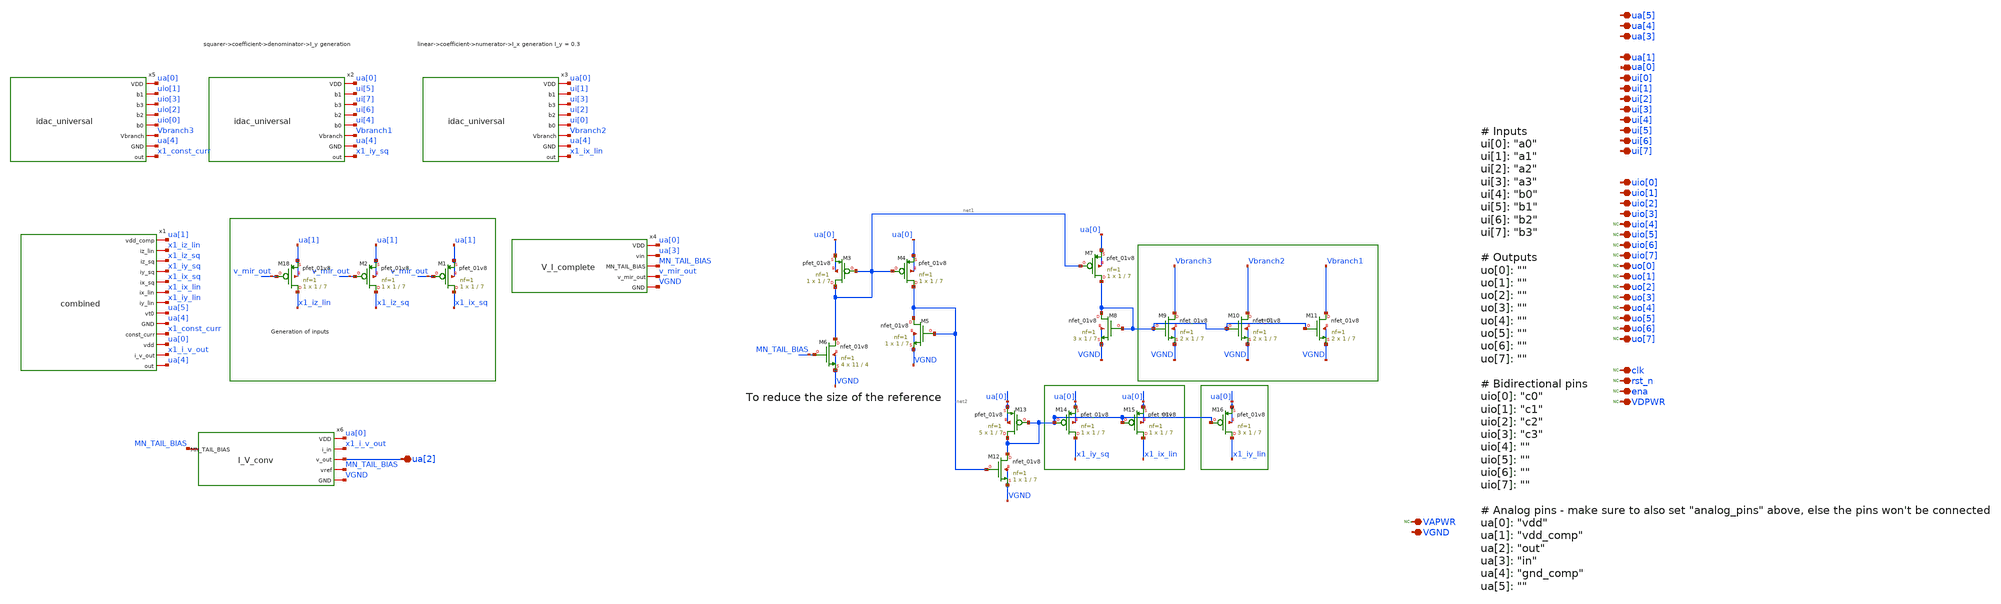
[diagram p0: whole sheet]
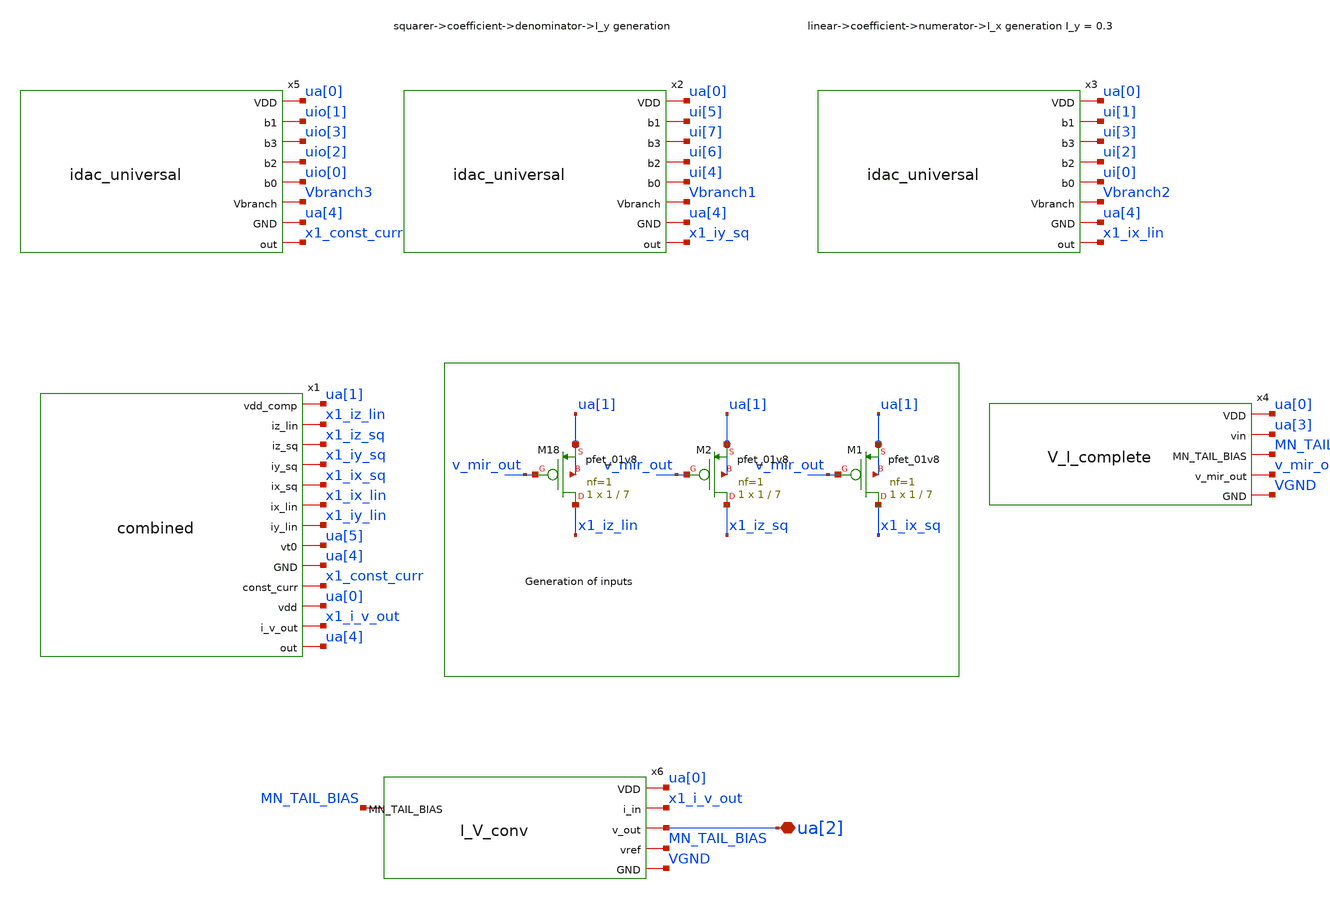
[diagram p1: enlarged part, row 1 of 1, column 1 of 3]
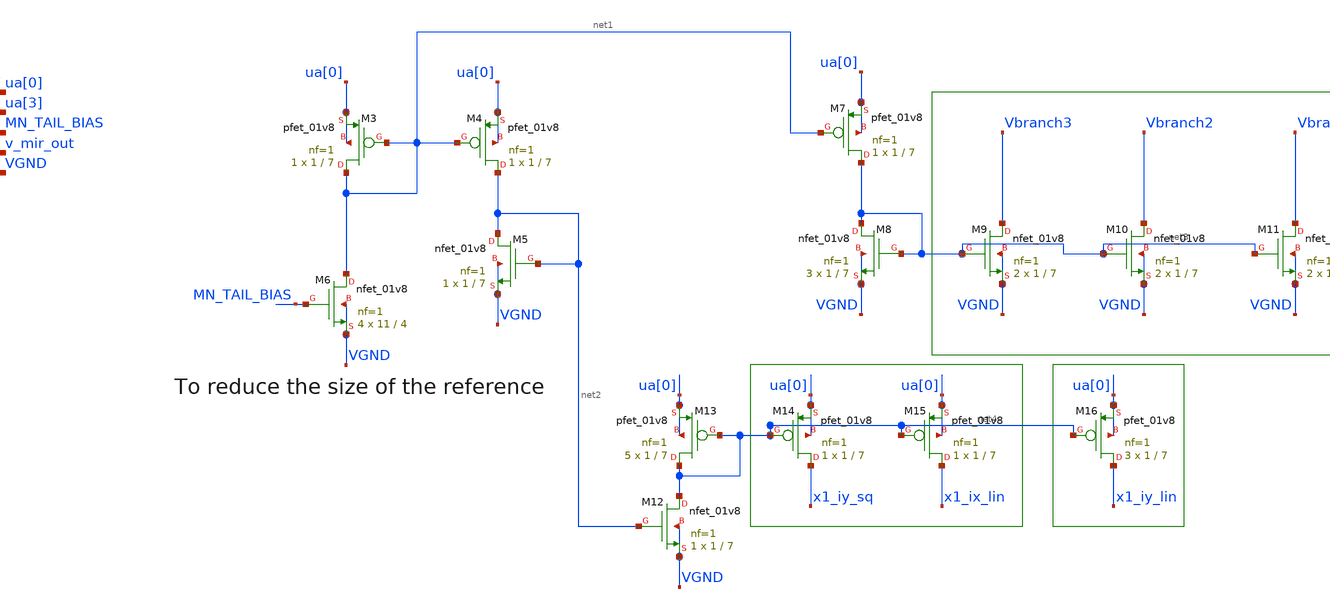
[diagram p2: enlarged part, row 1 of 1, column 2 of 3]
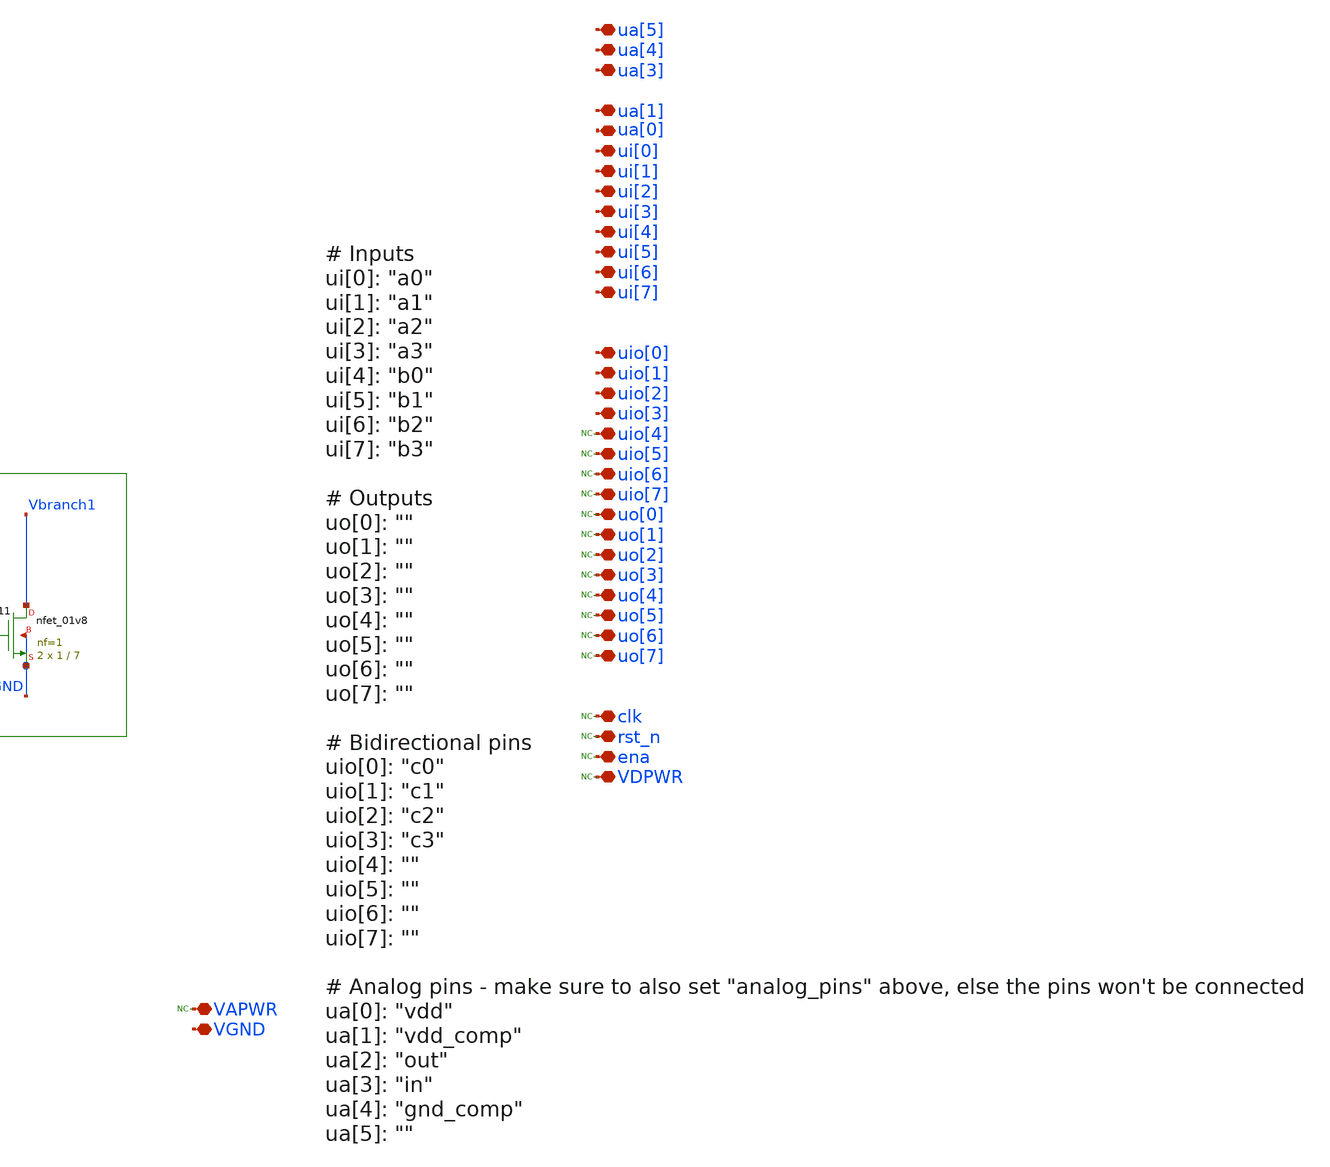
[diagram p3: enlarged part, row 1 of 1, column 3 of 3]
** sch_path: xschem/top/tt_um_psquared_analog_compute.sch
**.subckt tt_um_psquared_analog_compute ui[4] ui[5] ui[6] ui[7] uio[0] uio[1] uio[2] uio[3] uio[4]
*+ uio[5] uio[6] uio[7] uo[0] uo[1] uo[2] uo[3] uo[4] uo[5] uo[6] uo[7] clk rst_n ena ua[4] ua[5] ui[0] ui[3]
*+ ui[1] ui[2] VDPWR ua[3] ua[1] ua[0] VAPWR VGND ua[2]
*.iopin ui[4]
*.iopin ui[5]
*.iopin ui[6]
*.iopin ui[7]
*.iopin uio[0]
*.iopin uio[1]
*.iopin uio[2]
*.iopin uio[3]
*.iopin uio[4]
*.iopin uio[5]
*.iopin uio[6]
*.iopin uio[7]
*.iopin uo[0]
*.iopin uo[1]
*.iopin uo[2]
*.iopin uo[3]
*.iopin uo[4]
*.iopin uo[5]
*.iopin uo[6]
*.iopin uo[7]
*.iopin clk
*.iopin rst_n
*.iopin ena
*.iopin ua[4]
*.iopin ua[5]
*.iopin ui[0]
*.iopin ui[3]
*.iopin ui[1]
*.iopin ui[2]
*.iopin VDPWR
*.iopin ua[3]
*.iopin ua[1]
*.iopin ua[0]
*.iopin VAPWR
*.iopin VGND
*.iopin ua[2]
* noconn uio[4]
* noconn uio[5]
* noconn uio[6]
* noconn uio[7]
* noconn uo[0]
* noconn uo[1]
* noconn uo[2]
* noconn uo[3]
* noconn uo[4]
* noconn uo[5]
* noconn uo[6]
* noconn uo[7]
* noconn clk
* noconn rst_n
* noconn ena
* noconn VDPWR
x5 ua[0] uio[1] uio[3] uio[2] uio[0] Vbranch3 ua[4] x1_const_curr idac_universal
x2 ua[0] ui[5] ui[7] ui[6] ui[4] Vbranch1 ua[4] x1_iy_sq idac_universal
x3 ua[0] ui[1] ui[3] ui[2] ui[0] Vbranch2 ua[4] x1_ix_lin idac_universal
x1 ua[1] x1_iz_lin x1_iz_sq x1_iy_sq x1_ix_sq x1_ix_lin x1_iy_lin ua[5] ua[4] x1_const_curr ua[0]
+ x1_i_v_out ua[4] combined
x6 ua[0] x1_i_v_out ua[2] MN_TAIL_BIAS VGND MN_TAIL_BIAS I_V_conv
x4 ua[0] ua[3] MN_TAIL_BIAS v_mir_out VGND V_I_complete
XM6 net1 MN_TAIL_BIAS VGND VGND sky130_fd_pr__nfet_01v8 L=4 W=11 nf=1 ad='int((1 + 1)/2) * 11 / 1 * 0.29'
+ as='int((1 + 2)/2) * 11 / 1 * 0.29' pd='2*int((1 + 1)/2) * (11 / 1 + 0.29)' ps='2*int((1 + 2)/2) * (11 / 1 + 0.29)'
+ nrd='0.29 / 11 ' nrs='0.29 / 11 ' sa=0 sb=0 sd=0 mult=4 m=4
XM5 net2 net2 VGND VGND sky130_fd_pr__nfet_01v8 L=7 W=1 nf=1 ad='int((1 + 1)/2) * 1 / 1 * 0.29' as='int((1 + 2)/2) * 1 / 1 * 0.29'
+ pd='2*int((1 + 1)/2) * (1 / 1 + 0.29)' ps='2*int((1 + 2)/2) * (1 / 1 + 0.29)' nrd='0.29 / 1 ' nrs='0.29 / 1 '
+ sa=0 sb=0 sd=0 mult=1 m=1
XM12 net4 net2 VGND VGND sky130_fd_pr__nfet_01v8 L=7 W=1 nf=1 ad='int((1 + 1)/2) * 1 / 1 * 0.29' as='int((1 + 2)/2) * 1 / 1 * 0.29'
+ pd='2*int((1 + 1)/2) * (1 / 1 + 0.29)' ps='2*int((1 + 2)/2) * (1 / 1 + 0.29)' nrd='0.29 / 1 ' nrs='0.29 / 1 '
+ sa=0 sb=0 sd=0 mult=1 m=1
XM8 net3 net3 VGND VGND sky130_fd_pr__nfet_01v8 L=7 W=1 nf=1 ad='int((1 + 1)/2) * 1 / 1 * 0.29' as='int((1 + 2)/2) * 1 / 1 * 0.29'
+ pd='2*int((1 + 1)/2) * (1 / 1 + 0.29)' ps='2*int((1 + 2)/2) * (1 / 1 + 0.29)' nrd='0.29 / 1 ' nrs='0.29 / 1 '
+ sa=0 sb=0 sd=0 mult=3 m=3
XM9 Vbranch3 net3 VGND VGND sky130_fd_pr__nfet_01v8 L=7 W=1 nf=1 ad='int((1 + 1)/2) * 1 / 1 * 0.29' as='int((1 + 2)/2) * 1 / 1 * 0.29'
+ pd='2*int((1 + 1)/2) * (1 / 1 + 0.29)' ps='2*int((1 + 2)/2) * (1 / 1 + 0.29)' nrd='0.29 / 1 ' nrs='0.29 / 1 '
+ sa=0 sb=0 sd=0 mult=2 m=2
XM11 Vbranch1 net3 VGND VGND sky130_fd_pr__nfet_01v8 L=7 W=1 nf=1 ad='int((1 + 1)/2) * 1 / 1 * 0.29'
+ as='int((1 + 2)/2) * 1 / 1 * 0.29' pd='2*int((1 + 1)/2) * (1 / 1 + 0.29)' ps='2*int((1 + 2)/2) * (1 / 1 + 0.29)'
+ nrd='0.29 / 1 ' nrs='0.29 / 1 ' sa=0 sb=0 sd=0 mult=2 m=2
XM10 Vbranch2 net3 VGND VGND sky130_fd_pr__nfet_01v8 L=7 W=1 nf=1 ad='int((1 + 1)/2) * 1 / 1 * 0.29'
+ as='int((1 + 2)/2) * 1 / 1 * 0.29' pd='2*int((1 + 1)/2) * (1 / 1 + 0.29)' ps='2*int((1 + 2)/2) * (1 / 1 + 0.29)'
+ nrd='0.29 / 1 ' nrs='0.29 / 1 ' sa=0 sb=0 sd=0 mult=2 m=2
XM3 net1 net1 ua[0] ua[0] sky130_fd_pr__pfet_01v8 L=7 W=1 nf=1 ad='int((nf+1)/2) * W/nf * 0.29' as='int((nf+2)/2) * W/nf * 0.29'
+ pd='2*int((nf+1)/2) * (W/nf + 0.29)' ps='2*int((nf+2)/2) * (W/nf + 0.29)' nrd='0.29 / W' nrs='0.29 / W'
+ sa=0 sb=0 sd=0 mult=1 m=1
XM4 net2 net1 ua[0] ua[0] sky130_fd_pr__pfet_01v8 L=7 W=1 nf=1 ad='int((nf+1)/2) * W/nf * 0.29' as='int((nf+2)/2) * W/nf * 0.29'
+ pd='2*int((nf+1)/2) * (W/nf + 0.29)' ps='2*int((nf+2)/2) * (W/nf + 0.29)' nrd='0.29 / W' nrs='0.29 / W'
+ sa=0 sb=0 sd=0 mult=1 m=1
XM7 net3 net1 ua[0] ua[0] sky130_fd_pr__pfet_01v8 L=7 W=1 nf=1 ad='int((nf+1)/2) * W/nf * 0.29' as='int((nf+2)/2) * W/nf * 0.29'
+ pd='2*int((nf+1)/2) * (W/nf + 0.29)' ps='2*int((nf+2)/2) * (W/nf + 0.29)' nrd='0.29 / W' nrs='0.29 / W'
+ sa=0 sb=0 sd=0 mult=1 m=1
XM16 x1_iy_lin net4 ua[0] ua[0] sky130_fd_pr__pfet_01v8 L=7 W=1 nf=1 ad='int((nf+1)/2) * W/nf * 0.29'
+ as='int((nf+2)/2) * W/nf * 0.29' pd='2*int((nf+1)/2) * (W/nf + 0.29)' ps='2*int((nf+2)/2) * (W/nf + 0.29)'
+ nrd='0.29 / W' nrs='0.29 / W' sa=0 sb=0 sd=0 mult=3 m=3
XM15 x1_ix_lin net4 ua[0] ua[0] sky130_fd_pr__pfet_01v8 L=7 W=1 nf=1 ad='int((nf+1)/2) * W/nf * 0.29'
+ as='int((nf+2)/2) * W/nf * 0.29' pd='2*int((nf+1)/2) * (W/nf + 0.29)' ps='2*int((nf+2)/2) * (W/nf + 0.29)'
+ nrd='0.29 / W' nrs='0.29 / W' sa=0 sb=0 sd=0 mult=1 m=1
XM14 x1_iy_sq net4 ua[0] ua[0] sky130_fd_pr__pfet_01v8 L=7 W=1 nf=1 ad='int((nf+1)/2) * W/nf * 0.29'
+ as='int((nf+2)/2) * W/nf * 0.29' pd='2*int((nf+1)/2) * (W/nf + 0.29)' ps='2*int((nf+2)/2) * (W/nf + 0.29)'
+ nrd='0.29 / W' nrs='0.29 / W' sa=0 sb=0 sd=0 mult=1 m=1
XM13 net4 net4 ua[0] ua[0] sky130_fd_pr__pfet_01v8 L=7 W=1 nf=1 ad='int((nf+1)/2) * W/nf * 0.29' as='int((nf+2)/2) * W/nf * 0.29'
+ pd='2*int((nf+1)/2) * (W/nf + 0.29)' ps='2*int((nf+2)/2) * (W/nf + 0.29)' nrd='0.29 / W' nrs='0.29 / W'
+ sa=0 sb=0 sd=0 mult=5 m=5
XM1 x1_ix_sq v_mir_out ua[1] ua[1] sky130_fd_pr__pfet_01v8 L=7 W=1 nf=1 ad='int((nf+1)/2) * W/nf * 0.29'
+ as='int((nf+2)/2) * W/nf * 0.29' pd='2*int((nf+1)/2) * (W/nf + 0.29)' ps='2*int((nf+2)/2) * (W/nf + 0.29)'
+ nrd='0.29 / W' nrs='0.29 / W' sa=0 sb=0 sd=0 mult=1 m=1
XM2 x1_iz_sq v_mir_out ua[1] ua[1] sky130_fd_pr__pfet_01v8 L=7 W=1 nf=1 ad='int((nf+1)/2) * W/nf * 0.29'
+ as='int((nf+2)/2) * W/nf * 0.29' pd='2*int((nf+1)/2) * (W/nf + 0.29)' ps='2*int((nf+2)/2) * (W/nf + 0.29)'
+ nrd='0.29 / W' nrs='0.29 / W' sa=0 sb=0 sd=0 mult=1 m=1
XM18 x1_iz_lin v_mir_out ua[1] ua[1] sky130_fd_pr__pfet_01v8 L=7 W=1 nf=1 ad='int((nf+1)/2) * W/nf * 0.29'
+ as='int((nf+2)/2) * W/nf * 0.29' pd='2*int((nf+1)/2) * (W/nf + 0.29)' ps='2*int((nf+2)/2) * (W/nf + 0.29)'
+ nrd='0.29 / W' nrs='0.29 / W' sa=0 sb=0 sd=0 mult=1 m=1
* noconn VAPWR
**.ends
.end
